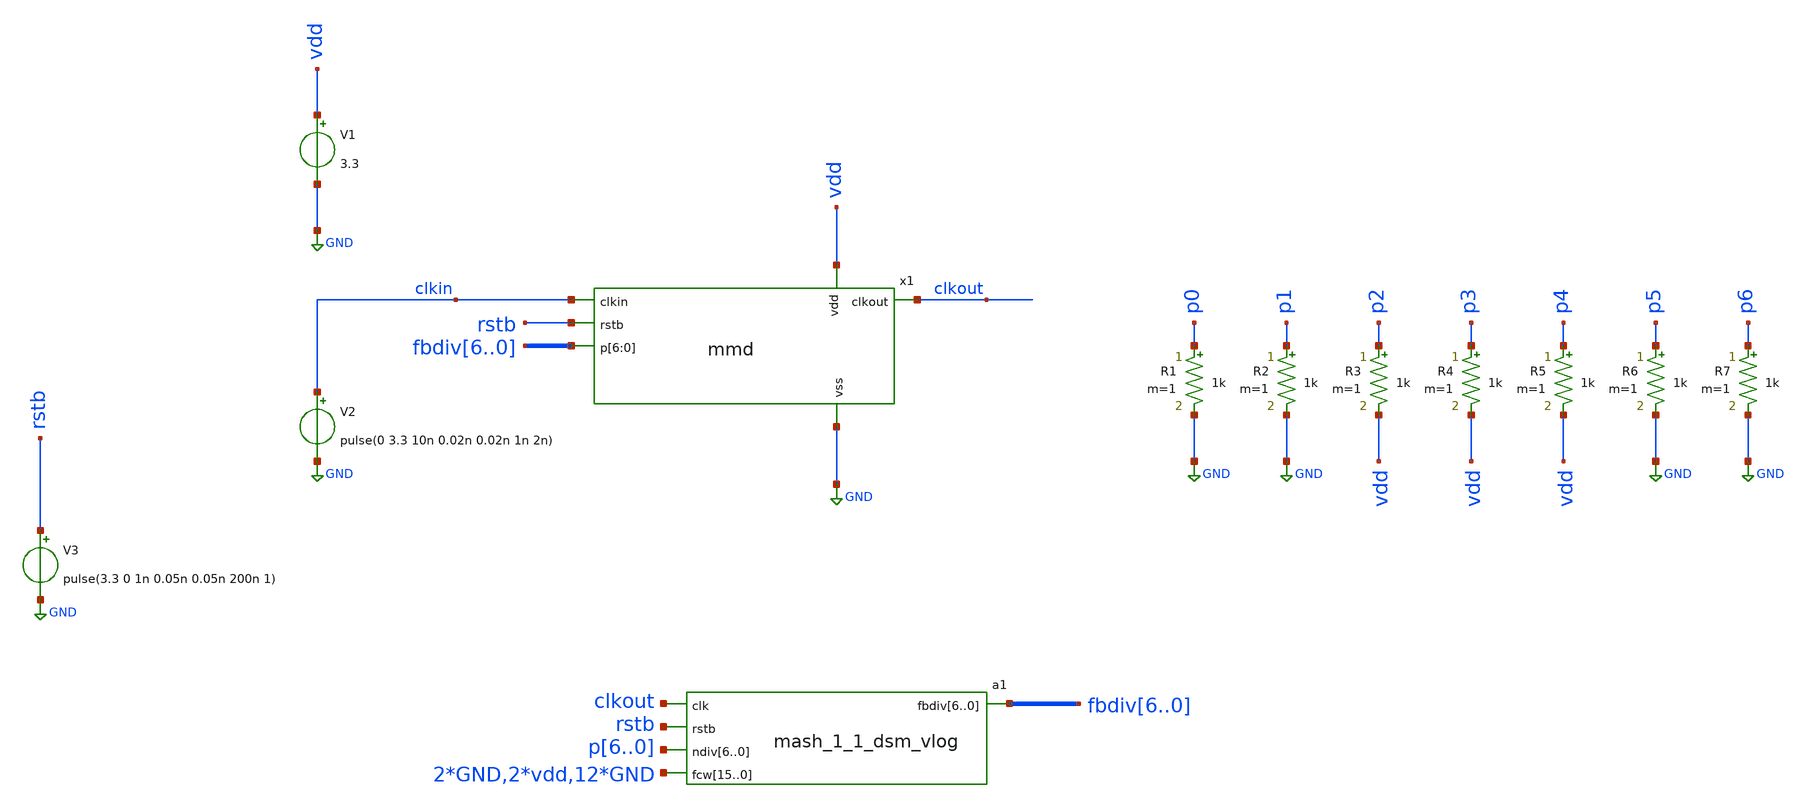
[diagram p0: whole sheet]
** sch_path: xschem/tb_mmd_vlog.sch
**.subckt tb_mmd_vlog
V2 clkin GND pulse(0 3.3 10n 0.02n 0.02n 1n 2n)
V1 vdd GND 3.3
V3 rstb GND pulse(3.3 0 1n 0.05n 0.05n 200n 1)
R1 p0 GND 1k m=1
R2 p1 GND 1k m=1
R3 p2 vdd 1k m=1
R4 p3 vdd 1k m=1
R5 p4 vdd 1k m=1
R6 p5 GND 1k m=1
R7 p6 GND 1k m=1
x1 clkout clkin vdd GND rstb fbdiv6 fbdiv5 fbdiv4 fbdiv3 fbdiv2 fbdiv1 fbdiv0 mmd
a1 [ clkout rstb p6 p5 p4 p3 p2 p1 p0 GND GND vdd vdd GND GND GND GND GND GND GND GND GND GND GND
+ GND ] [ fbdiv6 fbdiv5 fbdiv4 fbdiv3 fbdiv2 fbdiv1 fbdiv0 ] dut
**** begin user architecture code


.include /usr/local/share/pdk/gf180mcuD/libs.tech/ngspice/design.ngspice
.lib /usr/local/share/pdk/gf180mcuD/libs.tech/ngspice/sm141064.ngspice typical
.option temp=25
.ic v(vctrl_unfilt) = 1.3
.ic v(vctrlfb) = 1.3
.param VCC=3.3

.control
save all
tran 50p 0.6u
run
plot i(V1)
let clkin = v(clkin)
let clkout_plus_3p4 = v(clkout) + 3.4
plot clkin clkout_plus_3p4

.endc


**** end user architecture code
**.ends
.GLOBAL GND
**** begin user architecture code
.model dut d_cosim simulation="ivlng" sim_args=["mash_1_1_dsm"]
**** end user architecture code
.end
